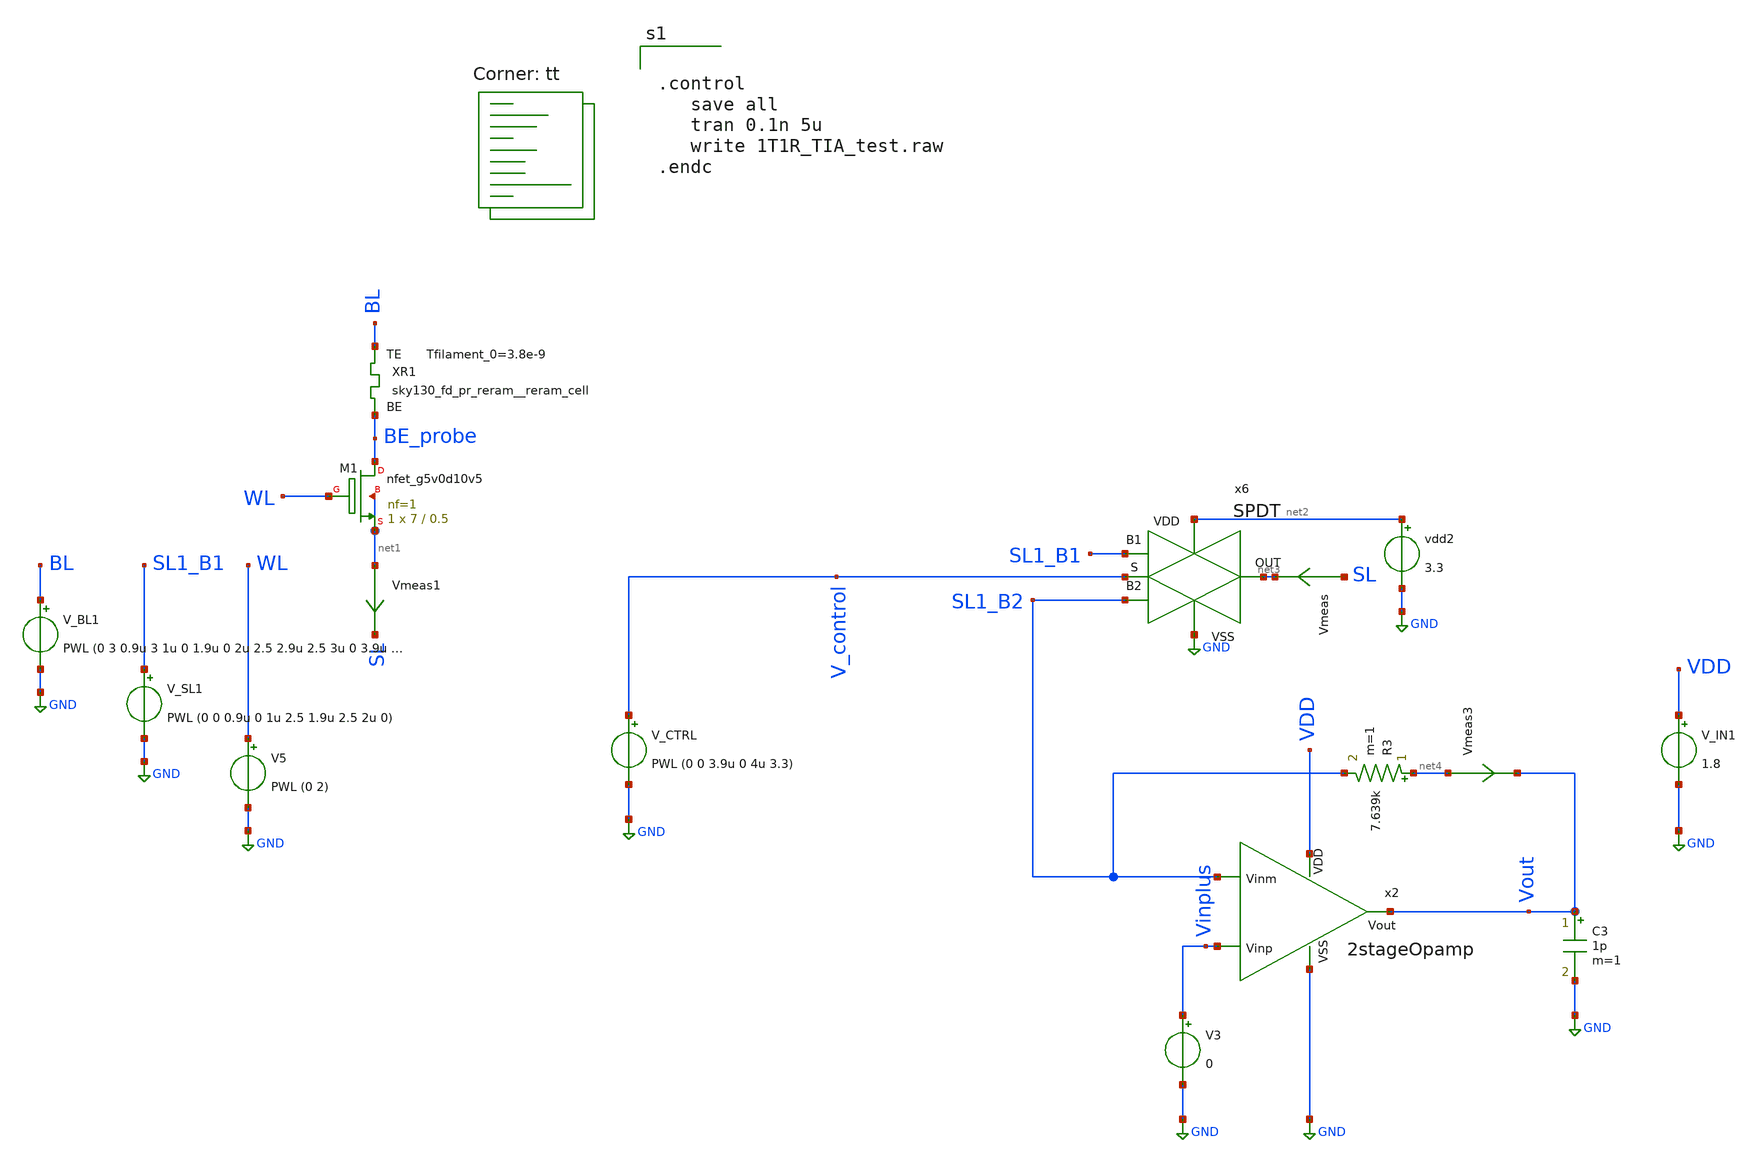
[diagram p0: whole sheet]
** sch_path: xschem/test/xschem/1T1R_TIA_test.sch
* StefanSchippers/xschem_sky130/sky130_fd_pr/reram.sym:
* Copyright 2021 Stefan Frederik Schippers
* Licensed under the Apache License, Version 2.0 (the "License");
**.subckt 1T1R_TIA_test
XR1 BL BE_probe sky130_fd_pr_reram__reram_cell Tfilament_0=3.8e-9
XM1 BE_probe WL net1 net1 sky130_fd_pr__nfet_g5v0d10v5 L=0.5 W=7 nf=1 ad='int((nf+1)/2) * W/nf * 0.29'
+ as='int((nf+2)/2) * W/nf * 0.29' pd='2*int((nf+1)/2) * (W/nf + 0.29)' ps='2*int((nf+2)/2) * (W/nf + 0.29)'
+ nrd='0.29 / W' nrs='0.29 / W' sa=0 sb=0 sd=0 mult=1 m=1
V_BL1 BL GND PWL (0 3 0.9u 3 1u 0 1.9u 0 2u 2.5 2.9u 2.5 3u 0 3.9u 0 4u 0.2)
V_SL1 SL1_B1 GND PWL (0 0 0.9u 0 1u 2.5 1.9u 2.5 2u 0)
V5 WL GND PWL (0 2)
Vmeas SL net3 0
.save i(vmeas)
x6 net2 GND SL1_B2 V_control SL1_B1 net3 SPDT
V_CTRL V_control GND PWL (0 0 3.9u 0 4u 3.3)
vdd2 net2 GND 3.3
Vmeas1 net1 SL 0
.save i(vmeas1)
x2 VDD SL1_B2 Vinplus Vout GND 2stageOpamp
R3 net4 SL1_B2 7.639k m=1
V3 Vinplus GND 0
Vmeas3 net4 Vout 0
.save i(vmeas3)
C3 Vout GND 1p m=1
V_IN1 VDD GND 1.8
**** begin user architecture code


.control
   save all
   tran 0.1n 5u
   write 1T1R_TIA_test.raw
.endc


.lib $::SKYWATER_MODELS/sky130.lib.spice tt
**** end user architecture code
**.ends

* expanding   symbol:  SPDT.sym # of pins=6
** sym_path: xschem/test/xschem/SPDT.sym
** sch_path: xschem/test/xschem/SPDT.sch
.subckt SPDT VDD VSS B2 S B1 OUT
*.ipin S
*.ipin VDD
*.ipin VSS
*.iopin OUT
*.iopin B1
*.iopin B2
XM1 OUT net1 B2 VSS sky130_fd_pr__nfet_g5v0d10v5 L=0.5 W=15 nf=1 ad='int((nf+1)/2) * W/nf * 0.29' as='int((nf+2)/2) * W/nf * 0.29'
+ pd='2*int((nf+1)/2) * (W/nf + 0.29)' ps='2*int((nf+2)/2) * (W/nf + 0.29)' nrd='0.29 / W' nrs='0.29 / W'
+ sa=0 sb=0 sd=0 mult=1 m=1
XM2 B2 net2 OUT VDD sky130_fd_pr__pfet_g5v0d10v5 L=0.5 W=15 nf=1 ad='int((nf+1)/2) * W/nf * 0.29' as='int((nf+2)/2) * W/nf * 0.29'
+ pd='2*int((nf+1)/2) * (W/nf + 0.29)' ps='2*int((nf+2)/2) * (W/nf + 0.29)' nrd='0.29 / W' nrs='0.29 / W'
+ sa=0 sb=0 sd=0 mult=1 m=1
XM3 OUT net2 B1 VSS sky130_fd_pr__nfet_g5v0d10v5 L=0.5 W=15 nf=1 ad='int((nf+1)/2) * W/nf * 0.29' as='int((nf+2)/2) * W/nf * 0.29'
+ pd='2*int((nf+1)/2) * (W/nf + 0.29)' ps='2*int((nf+2)/2) * (W/nf + 0.29)' nrd='0.29 / W' nrs='0.29 / W'
+ sa=0 sb=0 sd=0 mult=1 m=1
XM4 B1 net1 OUT VDD sky130_fd_pr__pfet_g5v0d10v5 L=0.5 W=15 nf=1 ad='int((nf+1)/2) * W/nf * 0.29' as='int((nf+2)/2) * W/nf * 0.29'
+ pd='2*int((nf+1)/2) * (W/nf + 0.29)' ps='2*int((nf+2)/2) * (W/nf + 0.29)' nrd='0.29 / W' nrs='0.29 / W'
+ sa=0 sb=0 sd=0 mult=1 m=1
XM5 net2 S VSS VSS sky130_fd_pr__nfet_g5v0d10v5 L=0.5 W=1 nf=1 ad='int((nf+1)/2) * W/nf * 0.29' as='int((nf+2)/2) * W/nf * 0.29'
+ pd='2*int((nf+1)/2) * (W/nf + 0.29)' ps='2*int((nf+2)/2) * (W/nf + 0.29)' nrd='0.29 / W' nrs='0.29 / W'
+ sa=0 sb=0 sd=0 mult=1 m=1
XM6 net2 S VDD VDD sky130_fd_pr__pfet_g5v0d10v5 L=0.5 W=1 nf=1 ad='int((nf+1)/2) * W/nf * 0.29' as='int((nf+2)/2) * W/nf * 0.29'
+ pd='2*int((nf+1)/2) * (W/nf + 0.29)' ps='2*int((nf+2)/2) * (W/nf + 0.29)' nrd='0.29 / W' nrs='0.29 / W'
+ sa=0 sb=0 sd=0 mult=1 m=1
XM7 net1 net2 VSS VSS sky130_fd_pr__nfet_g5v0d10v5 L=0.5 W=1 nf=1 ad='int((nf+1)/2) * W/nf * 0.29' as='int((nf+2)/2) * W/nf * 0.29'
+ pd='2*int((nf+1)/2) * (W/nf + 0.29)' ps='2*int((nf+2)/2) * (W/nf + 0.29)' nrd='0.29 / W' nrs='0.29 / W'
+ sa=0 sb=0 sd=0 mult=1 m=1
XM8 net1 net2 VDD VDD sky130_fd_pr__pfet_g5v0d10v5 L=0.5 W=1 nf=1 ad='int((nf+1)/2) * W/nf * 0.29' as='int((nf+2)/2) * W/nf * 0.29'
+ pd='2*int((nf+1)/2) * (W/nf + 0.29)' ps='2*int((nf+2)/2) * (W/nf + 0.29)' nrd='0.29 / W' nrs='0.29 / W'
+ sa=0 sb=0 sd=0 mult=1 m=1
.ends


* expanding   symbol:  amplifiers/dec24/2stageOpamp.sym # of pins=5
** sym_path: amplifiers/dec24/2stageOpamp.sym
** sch_path: amplifiers/dec24/2stageOpamp.sch
.subckt 2stageOpamp VDD Vinm Vinp Vout VSS
*.ipin Vinm
*.ipin Vinp
*.opin Vout
*.ipin VSS
*.ipin VDD
XM8 Vout net1 VSS VSS sky130_fd_pr__nfet_01v8 L=1 W=6 nf=1 ad='int((nf+1)/2) * W/nf * 0.29' as='int((nf+2)/2) * W/nf * 0.29'
+ pd='2*int((nf+1)/2) * (W/nf + 0.29)' ps='2*int((nf+2)/2) * (W/nf + 0.29)' nrd='0.29 / W' nrs='0.29 / W'
+ sa=0 sb=0 sd=0 mult=8 m=8
XM2 Vout Vb1 VDD VDD sky130_fd_pr__pfet_01v8_lvt L=1 W=9 nf=1 ad='int((nf+1)/2) * W/nf * 0.29' as='int((nf+2)/2) * W/nf * 0.29'
+ pd='2*int((nf+1)/2) * (W/nf + 0.29)' ps='2*int((nf+2)/2) * (W/nf + 0.29)' nrd='0.29 / W' nrs='0.29 / W'
+ sa=0 sb=0 sd=0 mult=3 m=3
XM5 net5 Vb3 net6 VSS sky130_fd_pr__nfet_01v8 L=1 W=4 nf=1 ad='int((nf+1)/2) * W/nf * 0.29' as='int((nf+2)/2) * W/nf * 0.29'
+ pd='2*int((nf+1)/2) * (W/nf + 0.29)' ps='2*int((nf+2)/2) * (W/nf + 0.29)' nrd='0.29 / W' nrs='0.29 / W'
+ sa=0 sb=0 sd=0 mult=3 m=3
XM17 net1 Vb3 net7 VSS sky130_fd_pr__nfet_01v8 L=1 W=4 nf=1 ad='int((nf+1)/2) * W/nf * 0.29' as='int((nf+2)/2) * W/nf * 0.29'
+ pd='2*int((nf+1)/2) * (W/nf + 0.29)' ps='2*int((nf+2)/2) * (W/nf + 0.29)' nrd='0.29 / W' nrs='0.29 / W'
+ sa=0 sb=0 sd=0 mult=3 m=3
XM3 net6 net5 VSS VSS sky130_fd_pr__nfet_01v8 L=1 W=8 nf=1 ad='int((nf+1)/2) * W/nf * 0.29' as='int((nf+2)/2) * W/nf * 0.29'
+ pd='2*int((nf+1)/2) * (W/nf + 0.29)' ps='2*int((nf+2)/2) * (W/nf + 0.29)' nrd='0.29 / W' nrs='0.29 / W'
+ sa=0 sb=0 sd=0 mult=1 m=1
XM19 net7 net5 VSS VSS sky130_fd_pr__nfet_01v8 L=1 W=8 nf=1 ad='int((nf+1)/2) * W/nf * 0.29' as='int((nf+2)/2) * W/nf * 0.29'
+ pd='2*int((nf+1)/2) * (W/nf + 0.29)' ps='2*int((nf+2)/2) * (W/nf + 0.29)' nrd='0.29 / W' nrs='0.29 / W'
+ sa=0 sb=0 sd=0 mult=1 m=1
V1 Vb1 GND 1.1
V2 Vb2 GND 0.7
V3 Vb3 GND 0.9
XM11 net8 Vb1 VDD VDD sky130_fd_pr__pfet_01v8_lvt L=1 W=9 nf=1 ad='int((nf+1)/2) * W/nf * 0.29' as='int((nf+2)/2) * W/nf * 0.29'
+ pd='2*int((nf+1)/2) * (W/nf + 0.29)' ps='2*int((nf+2)/2) * (W/nf + 0.29)' nrd='0.29 / W' nrs='0.29 / W'
+ sa=0 sb=0 sd=0 mult=2 m=2
XM1 net6 Vinm net8 VDD sky130_fd_pr__pfet_01v8_lvt L=1 W=8 nf=1 ad='int((nf+1)/2) * W/nf * 0.29' as='int((nf+2)/2) * W/nf * 0.29'
+ pd='2*int((nf+1)/2) * (W/nf + 0.29)' ps='2*int((nf+2)/2) * (W/nf + 0.29)' nrd='0.29 / W' nrs='0.29 / W'
+ sa=0 sb=0 sd=0 mult=3 m=3
XM15 net7 Vinp net8 VDD sky130_fd_pr__pfet_01v8_lvt L=1 W=8 nf=1 ad='int((nf+1)/2) * W/nf * 0.29' as='int((nf+2)/2) * W/nf * 0.29'
+ pd='2*int((nf+1)/2) * (W/nf + 0.29)' ps='2*int((nf+2)/2) * (W/nf + 0.29)' nrd='0.29 / W' nrs='0.29 / W'
+ sa=0 sb=0 sd=0 mult=3 m=3
XM7 net3 Vb1 VDD VDD sky130_fd_pr__pfet_01v8_lvt L=1 W=9 nf=1 ad='int((nf+1)/2) * W/nf * 0.29' as='int((nf+2)/2) * W/nf * 0.29'
+ pd='2*int((nf+1)/2) * (W/nf + 0.29)' ps='2*int((nf+2)/2) * (W/nf + 0.29)' nrd='0.29 / W' nrs='0.29 / W'
+ sa=0 sb=0 sd=0 mult=1 m=1
XM21 net4 Vb1 VDD VDD sky130_fd_pr__pfet_01v8_lvt L=1 W=9 nf=1 ad='int((nf+1)/2) * W/nf * 0.29' as='int((nf+2)/2) * W/nf * 0.29'
+ pd='2*int((nf+1)/2) * (W/nf + 0.29)' ps='2*int((nf+2)/2) * (W/nf + 0.29)' nrd='0.29 / W' nrs='0.29 / W'
+ sa=0 sb=0 sd=0 mult=1 m=1
XM9 net5 Vb2 net3 VDD sky130_fd_pr__pfet_01v8_lvt L=1 W=9 nf=1 ad='int((nf+1)/2) * W/nf * 0.29' as='int((nf+2)/2) * W/nf * 0.29'
+ pd='2*int((nf+1)/2) * (W/nf + 0.29)' ps='2*int((nf+2)/2) * (W/nf + 0.29)' nrd='0.29 / W' nrs='0.29 / W'
+ sa=0 sb=0 sd=0 mult=1 m=1
XM23 net1 Vb2 net4 VDD sky130_fd_pr__pfet_01v8_lvt L=1 W=9 nf=1 ad='int((nf+1)/2) * W/nf * 0.29' as='int((nf+2)/2) * W/nf * 0.29'
+ pd='2*int((nf+1)/2) * (W/nf + 0.29)' ps='2*int((nf+2)/2) * (W/nf + 0.29)' nrd='0.29 / W' nrs='0.29 / W'
+ sa=0 sb=0 sd=0 mult=1 m=1
XC4 net2 Vout sky130_fd_pr__cap_mim_m3_2 W=7 L=7 MF=4 m=4
R4 net1 net2 7k m=1
.ends

.GLOBAL GND
**** begin user architecture code

.subckt sky130_fd_pr_reram__reram_cell TE BE Tfilament_0=3.3e-9 area_ox=0.1024e-12
N1 TE BE nFilament sky130_fd_pr_reram__reram_model
.ic v(nFilament)={Tfilament_0*1.0e9}
.ends sky130_fd_pr_reram__reram_cell

.model sky130_fd_pr_reram__reram_model sky130_fd_pr_reram__reram_module  area_ox = 0.1024e-12  Tox =
+ 5.0  Tfilament_max = 4.9  Tfilament_min = 3.3  Eact_generation = 1.501  Eact_recombination  = 1.500
+  I_k1  = 6.140e-5  Tfilament_ref = 4.7249  V_ref = 0.430  velocity_k1 = 150  gamma_k0  = 16.5  gamma_k1
+  = -1.25  Temperature_0 = 300  C_thermal = 3.1825e-16  tau_thermal = 0.23e-9  t_step  = 1.0e-9
+  smoothing = 1e-7  Kclip = 200

.control
pre_osdi $SKYWATER_MODELS/sky130_fd_pr_reram__reram_module.osdi
.endc

**** end user architecture code
.end
